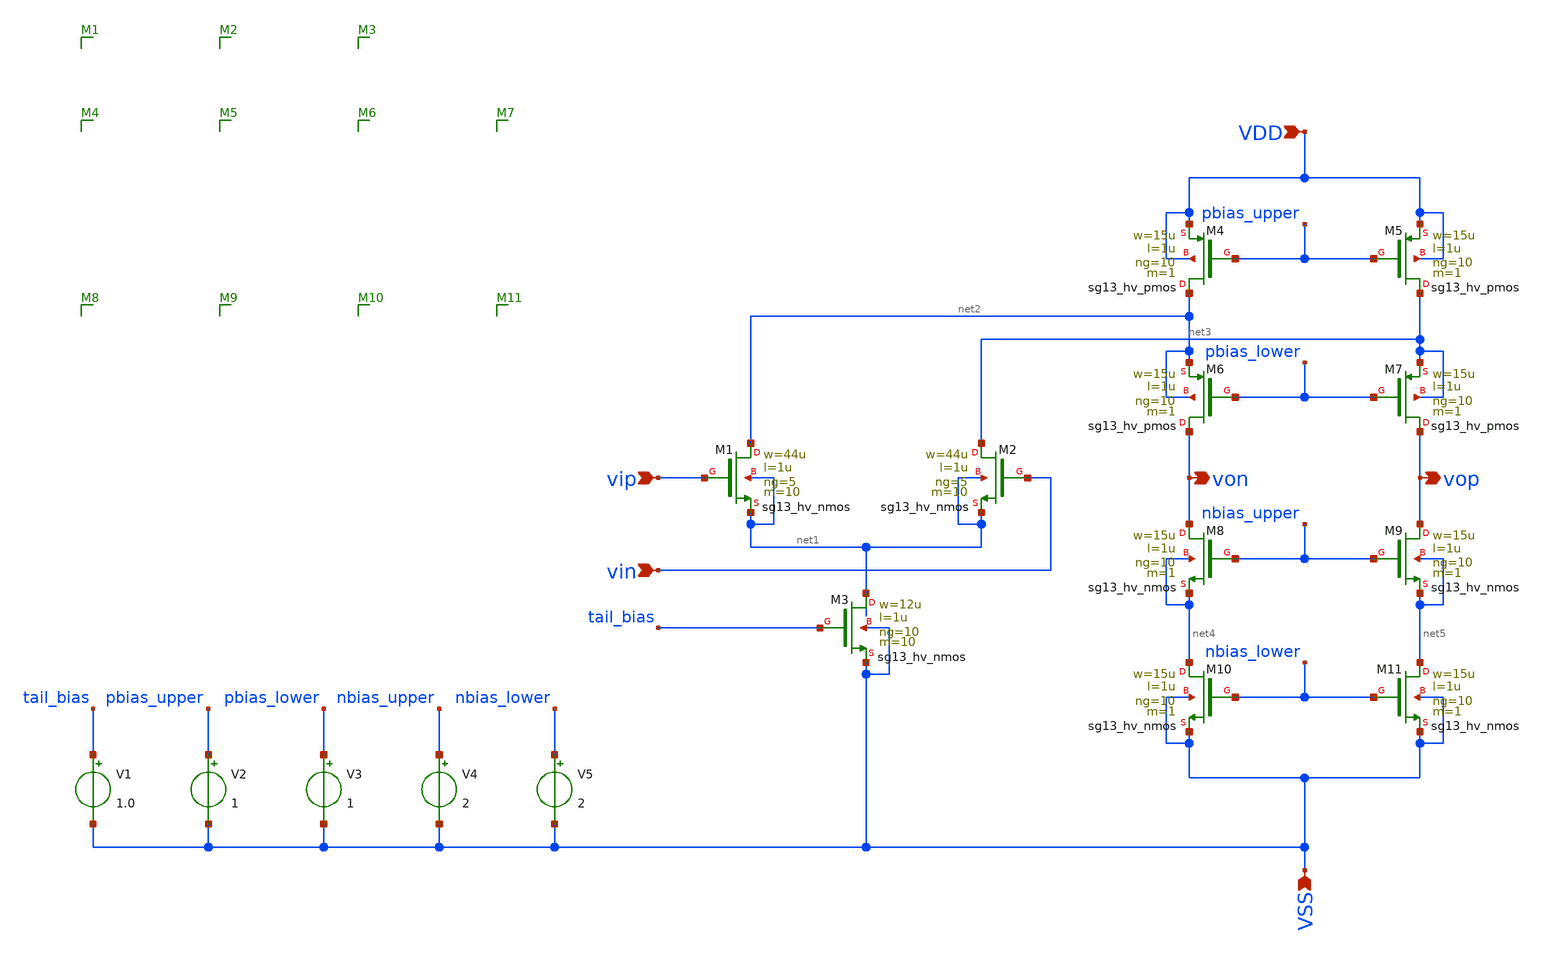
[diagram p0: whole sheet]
** sch_path: schematic/folded_cascode.sch
**.subckt folded_cascode VDD vip vin vop von VSS
*.ipin VDD
*.ipin vip
*.ipin vin
*.opin vop
*.opin von
*.ipin VSS
XM1 net2 vip net1 net1 sg13_hv_nmos w=44u l=1u ng=5 m=10 mm_ok=1
XM4 net2 pbias_upper VDD VDD sg13_hv_pmos w=15u l=1u ng=10 m=1 mm_ok=1
XM2 net3 vin net1 net1 sg13_hv_nmos w=44u l=1u ng=5 m=10 mm_ok=1
XM3 net1 tail_bias VSS VSS sg13_hv_nmos w=12u l=1u ng=10 m=10 mm_ok=1
XM5 net3 pbias_upper VDD VDD sg13_hv_pmos w=15u l=1u ng=10 m=1 mm_ok=1
XM6 von pbias_lower net2 net2 sg13_hv_pmos w=15u l=1u ng=10 m=1 mm_ok=1
XM7 vop pbias_lower net3 net3 sg13_hv_pmos w=15u l=1u ng=10 m=1 mm_ok=1
XM9 vop nbias_upper net5 net5 sg13_hv_nmos w=15u l=1u ng=10 m=1 mm_ok=1
XM8 von nbias_upper net4 net4 sg13_hv_nmos w=15u l=1u ng=10 m=1 mm_ok=1
XM11 net5 nbias_lower VSS VSS sg13_hv_nmos w=15u l=1u ng=10 m=1 mm_ok=1
XM10 net4 nbias_lower VSS VSS sg13_hv_nmos w=15u l=1u ng=10 m=1 mm_ok=1
V1 tail_bias VSS 1.0
V2 pbias_upper VSS 1
V3 pbias_lower VSS 1
V4 nbias_upper VSS 2
V5 nbias_lower VSS 2
**.ends
.end
